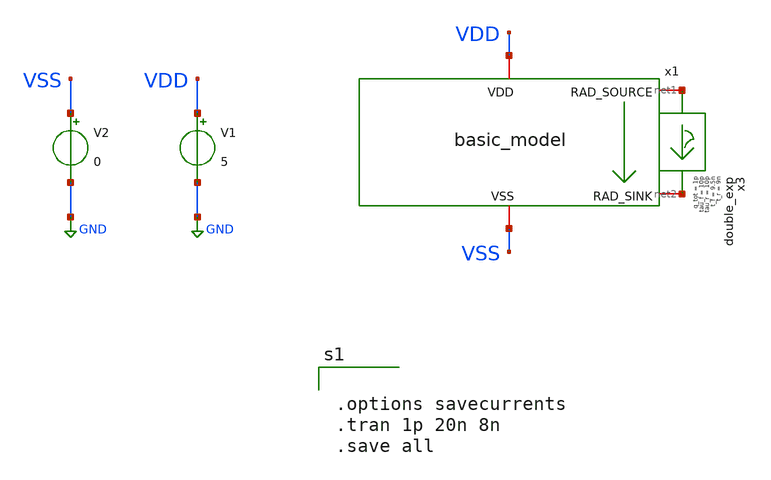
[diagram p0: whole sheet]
** sch_path: untitled-2.sch
**.subckt untitled-2
V1 VDD GND 5
V2 VSS GND 0
x3 net1 net2 double_exp t_r=9n tau_r=10p t_f=9.5n tau_f=10p q_tot=1p
x1 VDD net1 net2 VSS basic_model IS_N=1e-16 BF_N=100 VAF_N=100 IKF_N=0.1 CJE_N=2p CJC_N=2p TF_N=0.1n
+ TR_N=10n IS_P=1e-16 BF_P=100 VAF_P=100 IKF_P=0.1 CJE_P=2p CJC_P=2p TF_P=0.1n TR_P=10n
**** begin user architecture code


.options savecurrents
.tran 1p 20n 8n
.save all




.include /usr/local/share/rad_modeling_blocks/rad_modeling_blocks.spice


**** end user architecture code
**.ends

* expanding   symbol:  double_exp.sym # of pins=2
** sym_path: xschem_rad_library/double_exp.sym
** sch_path: xschem_rad_library/double_exp.sch
.subckt double_exp in out  t_r=0 t_f=0 tau_r=0 tau_f=0 q_tot=0
*.opin OUT
*.ipin IN
I1 IN OUT EXP(0 {q_tot / (t_f-t_r+tau_f-tau_r)} {t_r} {tau_r} {t_f} {tau_f})
.ends


* expanding   symbol:  OSCRE/latchup/basic_model.sym # of pins=4
** sym_path: latchup/basic_model.sym
** sch_path: latchup/basic_model.sch
.subckt basic_model VDD RAD_SOURCE RAD_SINK VSS   IS_N=1e-16  BF_N=100  VAF_N=100  IKF_N=0.1
+  CJE_N=2p  CJC_N=2p  TF_N=0.1n  TR_N=10n  IS_P=1e-16  BF_P=100  VAF_P=100  IKF_P=0.1  CJE_P=2p  CJC_P=2p
+  TF_P=0.1n  TR_P=10n
*.iopin VDD
*.iopin VSS
*.iopin RAD_SOURCE
*.iopin RAD_SINK
Q1 RAD_SINK RAD_SOURCE VDD pnp_cust area=1 m=1
Q2 RAD_SOURCE RAD_SINK VSS npn_cust area=1 m=1
R3 RAD_SINK VSS 50 m=1
R4 VDD RAD_SOURCE 50 m=1
**** begin user architecture code


.model npn_cust npn (IS={IS_N} BF={BF_N} VAF={VAF_N} IKF={IKF_N} CJE={CJE_N} CJC={CJC_N} TF={TF_N} TR={TR_N})
.model pnp_cust pnp (IS=1e-16 BF=100 VAF=100 IKF=0.1 CJE=2p CJC=2p TF=0.1n TR=10n)


**** end user architecture code
.ends

.GLOBAL GND
.end
